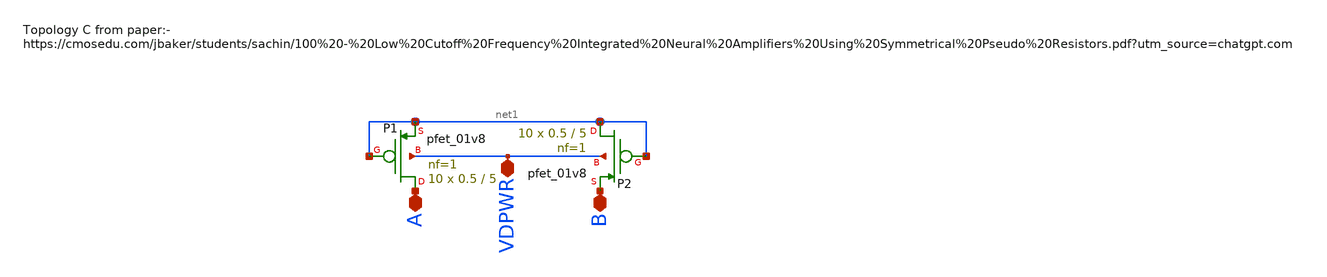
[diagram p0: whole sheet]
** sch_path: xschem/pseudo_res_c.sch
**.subckt pseudo_res_c A B VDPWR
*.iopin A
*.iopin B
*.iopin VDPWR
XP1 A net1 net1 VDPWR sky130_fd_pr__pfet_01v8 L=5 W=0.5 nf=1 ad='int((1 + 1)/2) * 0.5 / 1 * 0.29' as='int((1 + 2)/2) * 0.5 / 1 * 0.29'
+ pd='2*int((1 + 1)/2) * (0.5 / 1 + 0.29)' ps='2*int((1 + 2)/2) * (0.5 / 1 + 0.29)' nrd='0.29 / 0.5 ' nrs='0.29 / 0.5 '
+ sa=0 sb=0 sd=0 mult=10 m=10
XP2 net1 net1 B VDPWR sky130_fd_pr__pfet_01v8 L=5 W=0.5 nf=1 ad='int((1 + 1)/2) * 0.5 / 1 * 0.29' as='int((1 + 2)/2) * 0.5 / 1 * 0.29'
+ pd='2*int((1 + 1)/2) * (0.5 / 1 + 0.29)' ps='2*int((1 + 2)/2) * (0.5 / 1 + 0.29)' nrd='0.29 / 0.5 ' nrs='0.29 / 0.5 '
+ sa=0 sb=0 sd=0 mult=10 m=10
**.ends
.end
